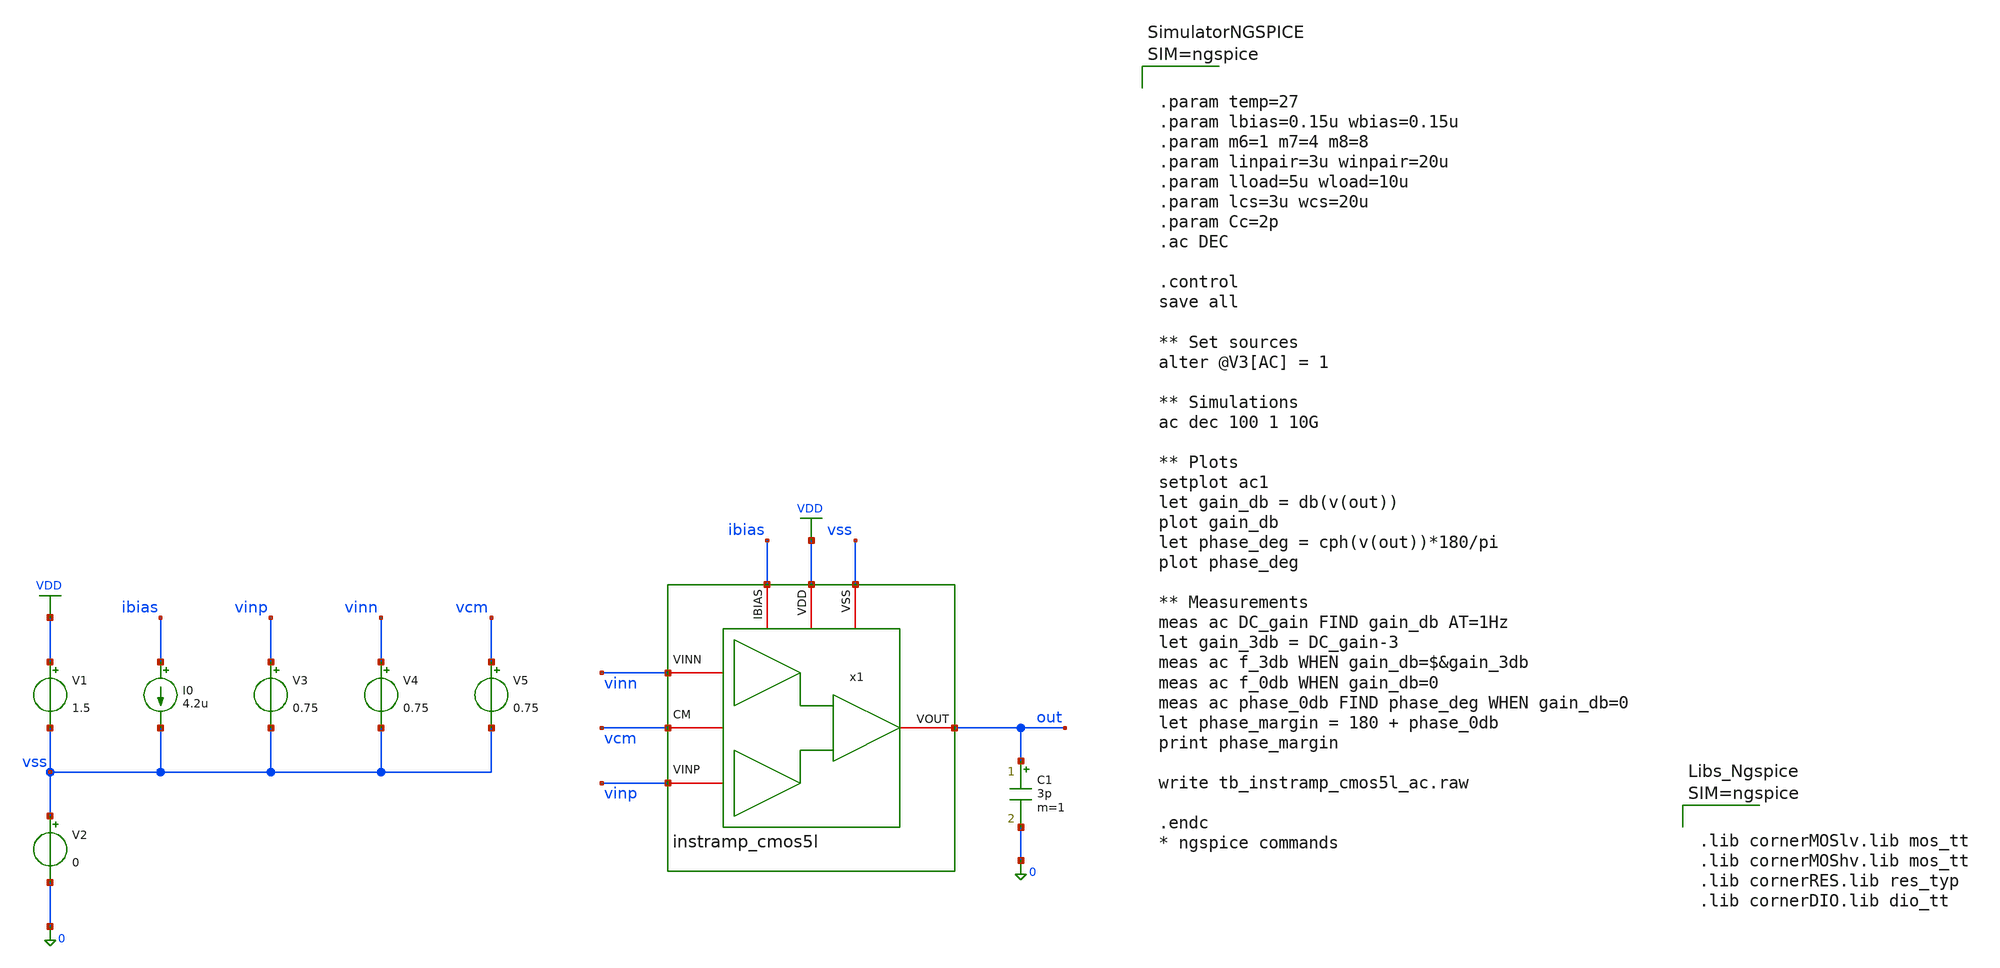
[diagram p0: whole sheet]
** sch_path: designs/libs/tb_analog/tb_instramp_cmos5l_ac/tb_instramp_cmos5l_ac.sch
**.subckt tb_instramp_cmos5l_ac
C1 out 0 3p m=1
I0 ibias vss 4.2u
V1 VDD vss 1.5
V2 vss 0 0
V3 vinp vss 0.75
V4 vinn vss 0.75
x1 vss VDD ibias vinn out vinp vcm instramp_cmos5l
V5 vcm vss 0.75
**** begin user architecture code



.param temp=27
.param lbias=0.15u wbias=0.15u
.param m6=1 m7=4 m8=8
.param linpair=3u winpair=20u
.param lload=5u wload=10u
.param lcs=3u wcs=20u
.param Cc=2p
.ac DEC

.control
save all

** Set sources
alter @V3[AC] = 1

** Simulations
ac dec 100 1 10G

** Plots
setplot ac1
let gain_db = db(v(out))
plot gain_db
let phase_deg = cph(v(out))*180/pi
plot phase_deg

** Measurements
meas ac DC_gain FIND gain_db AT=1Hz
let gain_3db = DC_gain-3
meas ac f_3db WHEN gain_db=$&gain_3db
meas ac f_0db WHEN gain_db=0
meas ac phase_0db FIND phase_deg WHEN gain_db=0
let phase_margin = 180 + phase_0db
print phase_margin

write tb_instramp_cmos5l_ac.raw

.endc
* ngspice commands






.lib cornerMOSlv.lib mos_tt
.lib cornerMOShv.lib mos_tt
.lib cornerRES.lib res_typ
.lib cornerDIO.lib dio_tt



**** end user architecture code
**.ends

* expanding   symbol:
*+  /foss/designs/Programmable-Instrumentation-Amplifier-IP/designs/libs/core_analog/instramp_cmos5l/instramp_cmos5l.sym # of pins=7
** sym_path: designs/libs/core_analog/instramp_cmos5l/instramp_cmos5l.sym
** sch_path: designs/libs/core_analog/instramp_cmos5l/instramp_cmos5l.sch
.subckt instramp_cmos5l VSS VDD IBIAS VINN VOUT VINP CM
*.iopin VDD
*.iopin IBIAS
*.iopin VSS
*.iopin CM
*.iopin VOUT
*.iopin VINN
*.iopin VINP
x1 vss ibias vdd net3 VINP net4 ota_cmos5l
x2 vss ibias vdd net1 VINN net2 ota_cmos5l
x3 vss ibias vdd net5 net6 net8 ota_cmos5l
XR1 net4 net6 sub! rhigh w=0.5e-6 l=2e-6 m=1 b=0 mm_ok=1
XR2 net2 net5 sub! rhigh w=0.5e-6 l=2e-6 m=1 b=0 mm_ok=1
XR3 net6 CM sub! rhigh w=0.5e-6 l=8*2.1e-6 m=1 b=0 mm_ok=1
XR4 net5 net7 sub! rhigh w=0.5e-6 l=8*2.1e-6 m=1 b=0 mm_ok=1
Vmeas net7 net8 0
.save i(vmeas)
Vmeas1 net8 VOUT 0
.save i(vmeas1)
R5 VINN vcm 10MEG m=1
R6 vcm VINP 10MEG m=1
XR7 net2 net1 sub! rhigh w=0.5e-6 l=2e-6 m=1 b=0 mm_ok=1
XR8 net4 net3 sub! rhigh w=0.5e-6 l=2e-6 m=1 b=0 mm_ok=1
.ends


* expanding   symbol:
*+  /foss/designs/Programmable-Instrumentation-Amplifier-IP/designs/libs/core_analog/ota_cmos5l/ota_cmos5l.sym # of pins=6
** sym_path: /foss/designs/Programmable-Instrumentation-Amplifier-IP/designs/libs/core_analog/ota_cmos5l/ota_cmos5l.sym
** sch_path: /foss/designs/Programmable-Instrumentation-Amplifier-IP/designs/libs/core_analog/ota_cmos5l/ota_cmos5l.sch
.subckt ota_cmos5l VSS IBIAS VDD VINN VINP VOUT
*.iopin IBIAS
*.iopin VDD
*.iopin VSS
*.iopin VOUT
*.iopin VINP
*.iopin VINN
XM6 net1 net1 vdd vdd sg13_lv_pmos w={wbias} l={lbias} ng=1 m={m6} mm_ok=1
XM7 net5 net1 vdd vdd sg13_lv_pmos w={wbias} l={lbias} ng=1 m={m7} mm_ok=1
XM8 net6 net1 vdd vdd sg13_lv_pmos w={wbias} l={lbias} ng=1 m={m8} mm_ok=1
XM1 net7 VINN net2 vdd sg13_lv_pmos w={winpair} l={linpair} ng=1 m=1 mm_ok=1
XM2 net8 VINP net2 vdd sg13_lv_pmos w={winpair} l={linpair} ng=1 m=1 mm_ok=1
XM3 net3 net3 gnd gnd sg13_lv_nmos w={wload} l={lload} ng=1 m=1 mm_ok=1
XM4 net4 net3 gnd gnd sg13_lv_nmos w={wload} l={lload} ng=1 m=1 mm_ok=1
XM5 net9 net4 gnd gnd sg13_lv_nmos w={wcs} l={lcs} ng=1 m=1 mm_ok=1
C1 net10 net9 {Cc} m=1
XR1 net4 net10 sub! rhigh w=0.5e-6 l=1.95e-6 m=1 b=0 mm_ok=1
**** begin user architecture code



.include ota_cmos5l.save
.param temp=27
.param lbias=0.15u wbias=0.15u
.param m6=1 m7=4 m8=10
.param linpair=3u winpair=20u
.param lload=0.5u wload=0.42u
.param lcs=5u wcs=19.13u
.param Cc=1.5p
.control
op
write ota_cmos5l.raw
.endc



**** end user architecture code
**** begin user architecture code



.lib cornerMOSlv.lib mos_tt
.lib cornerMOShv.lib mos_tt
.lib cornerRES.lib res_typ
.lib cornerDIO.lib dio_tt



**** end user architecture code
VIBIAS net1 ibias 0
.save i(vibias)
VID7 net5 net2 0
.save i(vid7)
VID8 net6 VOUT 0
.save i(vid8)
VIVDD VDD vdd 0
.save i(vivdd)
.save v(vinp)
.save v(vinn)
.save v(vout)
VID1 net7 net3 0
.save i(vid1)
VID2 net8 net4 0
.save i(vid2)
VID5 VOUT net9 0
.save i(vid5)
.ends

.GLOBAL VDD
.end
